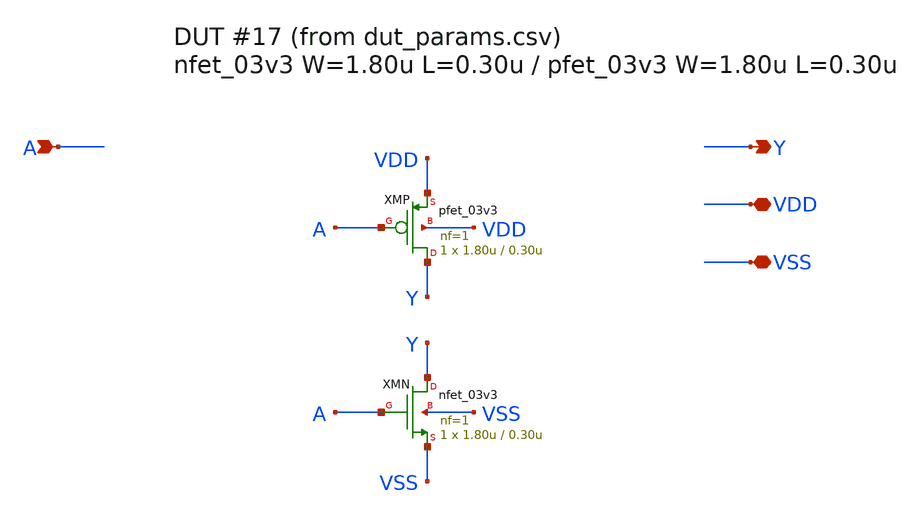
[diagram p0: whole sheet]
** sch_path: inverter_matrix/dut/inv_dut_017.sch
**.subckt inv_dut_017 A Y VDD VSS
*.ipin A
*.opin Y
*.iopin VDD
*.iopin VSS
XMP Y A VDD VDD pfet_03v3 L=0.30u W=1.80u nf=1 ad='int((nf+1)/2) * W/nf * 0.18u' as='int((nf+2)/2) * W/nf * 0.18u'
+ pd='2*int((nf+1)/2) * (W/nf + 0.18u)' ps='2*int((nf+2)/2) * (W/nf + 0.18u)' nrd='0.18u / W' nrs='0.18u / W'
+ sa=0 sb=0 sd=0 m=1
XMN Y A VSS VSS nfet_03v3 L=0.30u W=1.80u nf=1 ad='int((nf+1)/2) * W/nf * 0.18u' as='int((nf+2)/2) * W/nf * 0.18u'
+ pd='2*int((nf+1)/2) * (W/nf + 0.18u)' ps='2*int((nf+2)/2) * (W/nf + 0.18u)' nrd='0.18u / W' nrs='0.18u / W'
+ sa=0 sb=0 sd=0 m=1
**.ends
.end
